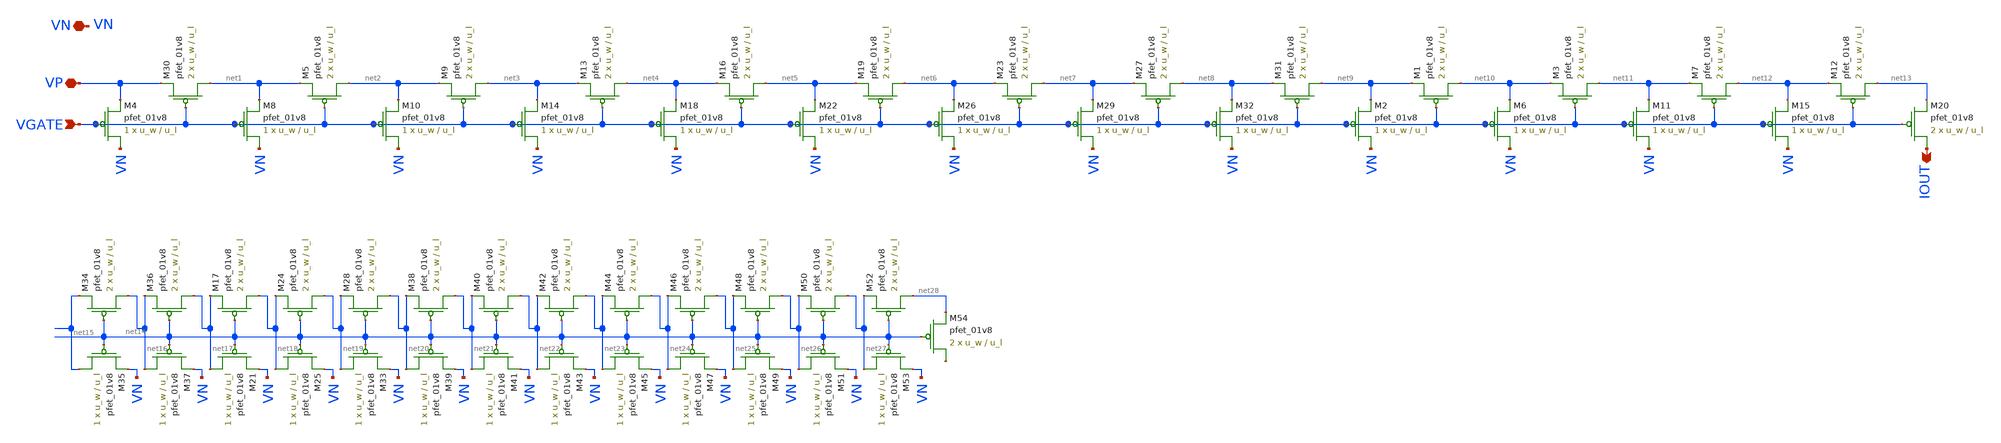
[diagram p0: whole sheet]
** sch_path: lib/analog/schematic/current_divider_original.sch
**.subckt current_divider_original VGATE VP VN IOUT
*.ipin VGATE
*.iopin VP
*.iopin VN
*.opin IOUT
XM30 net1 VGATE VP VDD sky130_fd_pr__pfet_01v8 L=u_l W=u_w nf=1 ad='int((nf+1)/2) * W/nf * 0.29' as='int((nf+2)/2) * W/nf * 0.29'
+ pd='2*int((nf+1)/2) * (W/nf + 0.29)' ps='2*int((nf+2)/2) * (W/nf + 0.29)' nrd='0.29 / W' nrs='0.29 / W'
+ sa=0 sb=0 sd=0 mult=2 m=2
XM4 VN VGATE VP VDD sky130_fd_pr__pfet_01v8 L=u_l W=u_w nf=1 ad='int((nf+1)/2) * W/nf * 0.29' as='int((nf+2)/2) * W/nf * 0.29'
+ pd='2*int((nf+1)/2) * (W/nf + 0.29)' ps='2*int((nf+2)/2) * (W/nf + 0.29)' nrd='0.29 / W' nrs='0.29 / W'
+ sa=0 sb=0 sd=0 mult=1 m=1
XM5 net2 VGATE net1 VDD sky130_fd_pr__pfet_01v8 L=u_l W=u_w nf=1 ad='int((nf+1)/2) * W/nf * 0.29' as='int((nf+2)/2) * W/nf * 0.29'
+ pd='2*int((nf+1)/2) * (W/nf + 0.29)' ps='2*int((nf+2)/2) * (W/nf + 0.29)' nrd='0.29 / W' nrs='0.29 / W'
+ sa=0 sb=0 sd=0 mult=2 m=2
XM8 VN VGATE net1 VDD sky130_fd_pr__pfet_01v8 L=u_l W=u_w nf=1 ad='int((nf+1)/2) * W/nf * 0.29' as='int((nf+2)/2) * W/nf * 0.29'
+ pd='2*int((nf+1)/2) * (W/nf + 0.29)' ps='2*int((nf+2)/2) * (W/nf + 0.29)' nrd='0.29 / W' nrs='0.29 / W'
+ sa=0 sb=0 sd=0 mult=1 m=1
XM9 net3 VGATE net2 VDD sky130_fd_pr__pfet_01v8 L=u_l W=u_w nf=1 ad='int((nf+1)/2) * W/nf * 0.29' as='int((nf+2)/2) * W/nf * 0.29'
+ pd='2*int((nf+1)/2) * (W/nf + 0.29)' ps='2*int((nf+2)/2) * (W/nf + 0.29)' nrd='0.29 / W' nrs='0.29 / W'
+ sa=0 sb=0 sd=0 mult=2 m=2
XM10 VN VGATE net2 VDD sky130_fd_pr__pfet_01v8 L=u_l W=u_w nf=1 ad='int((nf+1)/2) * W/nf * 0.29' as='int((nf+2)/2) * W/nf * 0.29'
+ pd='2*int((nf+1)/2) * (W/nf + 0.29)' ps='2*int((nf+2)/2) * (W/nf + 0.29)' nrd='0.29 / W' nrs='0.29 / W'
+ sa=0 sb=0 sd=0 mult=1 m=1
XM13 net4 VGATE net3 VDD sky130_fd_pr__pfet_01v8 L=u_l W=u_w nf=1 ad='int((nf+1)/2) * W/nf * 0.29' as='int((nf+2)/2) * W/nf * 0.29'
+ pd='2*int((nf+1)/2) * (W/nf + 0.29)' ps='2*int((nf+2)/2) * (W/nf + 0.29)' nrd='0.29 / W' nrs='0.29 / W'
+ sa=0 sb=0 sd=0 mult=2 m=2
XM14 VN VGATE net3 VDD sky130_fd_pr__pfet_01v8 L=u_l W=u_w nf=1 ad='int((nf+1)/2) * W/nf * 0.29' as='int((nf+2)/2) * W/nf * 0.29'
+ pd='2*int((nf+1)/2) * (W/nf + 0.29)' ps='2*int((nf+2)/2) * (W/nf + 0.29)' nrd='0.29 / W' nrs='0.29 / W'
+ sa=0 sb=0 sd=0 mult=1 m=1
XM16 net5 VGATE net4 VDD sky130_fd_pr__pfet_01v8 L=u_l W=u_w nf=1 ad='int((nf+1)/2) * W/nf * 0.29' as='int((nf+2)/2) * W/nf * 0.29'
+ pd='2*int((nf+1)/2) * (W/nf + 0.29)' ps='2*int((nf+2)/2) * (W/nf + 0.29)' nrd='0.29 / W' nrs='0.29 / W'
+ sa=0 sb=0 sd=0 mult=2 m=2
XM18 VN VGATE net4 VDD sky130_fd_pr__pfet_01v8 L=u_l W=u_w nf=1 ad='int((nf+1)/2) * W/nf * 0.29' as='int((nf+2)/2) * W/nf * 0.29'
+ pd='2*int((nf+1)/2) * (W/nf + 0.29)' ps='2*int((nf+2)/2) * (W/nf + 0.29)' nrd='0.29 / W' nrs='0.29 / W'
+ sa=0 sb=0 sd=0 mult=1 m=1
XM19 net6 VGATE net5 VDD sky130_fd_pr__pfet_01v8 L=u_l W=u_w nf=1 ad='int((nf+1)/2) * W/nf * 0.29' as='int((nf+2)/2) * W/nf * 0.29'
+ pd='2*int((nf+1)/2) * (W/nf + 0.29)' ps='2*int((nf+2)/2) * (W/nf + 0.29)' nrd='0.29 / W' nrs='0.29 / W'
+ sa=0 sb=0 sd=0 mult=2 m=2
XM22 VN VGATE net5 VDD sky130_fd_pr__pfet_01v8 L=u_l W=u_w nf=1 ad='int((nf+1)/2) * W/nf * 0.29' as='int((nf+2)/2) * W/nf * 0.29'
+ pd='2*int((nf+1)/2) * (W/nf + 0.29)' ps='2*int((nf+2)/2) * (W/nf + 0.29)' nrd='0.29 / W' nrs='0.29 / W'
+ sa=0 sb=0 sd=0 mult=1 m=1
XM23 net7 VGATE net6 VDD sky130_fd_pr__pfet_01v8 L=u_l W=u_w nf=1 ad='int((nf+1)/2) * W/nf * 0.29' as='int((nf+2)/2) * W/nf * 0.29'
+ pd='2*int((nf+1)/2) * (W/nf + 0.29)' ps='2*int((nf+2)/2) * (W/nf + 0.29)' nrd='0.29 / W' nrs='0.29 / W'
+ sa=0 sb=0 sd=0 mult=2 m=2
XM26 VN VGATE net6 VDD sky130_fd_pr__pfet_01v8 L=u_l W=u_w nf=1 ad='int((nf+1)/2) * W/nf * 0.29' as='int((nf+2)/2) * W/nf * 0.29'
+ pd='2*int((nf+1)/2) * (W/nf + 0.29)' ps='2*int((nf+2)/2) * (W/nf + 0.29)' nrd='0.29 / W' nrs='0.29 / W'
+ sa=0 sb=0 sd=0 mult=1 m=1
XM27 net8 VGATE net7 VDD sky130_fd_pr__pfet_01v8 L=u_l W=u_w nf=1 ad='int((nf+1)/2) * W/nf * 0.29' as='int((nf+2)/2) * W/nf * 0.29'
+ pd='2*int((nf+1)/2) * (W/nf + 0.29)' ps='2*int((nf+2)/2) * (W/nf + 0.29)' nrd='0.29 / W' nrs='0.29 / W'
+ sa=0 sb=0 sd=0 mult=2 m=2
XM29 VN VGATE net7 VDD sky130_fd_pr__pfet_01v8 L=u_l W=u_w nf=1 ad='int((nf+1)/2) * W/nf * 0.29' as='int((nf+2)/2) * W/nf * 0.29'
+ pd='2*int((nf+1)/2) * (W/nf + 0.29)' ps='2*int((nf+2)/2) * (W/nf + 0.29)' nrd='0.29 / W' nrs='0.29 / W'
+ sa=0 sb=0 sd=0 mult=1 m=1
XM31 net9 VGATE net8 VDD sky130_fd_pr__pfet_01v8 L=u_l W=u_w nf=1 ad='int((nf+1)/2) * W/nf * 0.29' as='int((nf+2)/2) * W/nf * 0.29'
+ pd='2*int((nf+1)/2) * (W/nf + 0.29)' ps='2*int((nf+2)/2) * (W/nf + 0.29)' nrd='0.29 / W' nrs='0.29 / W'
+ sa=0 sb=0 sd=0 mult=2 m=2
XM32 VN VGATE net8 VDD sky130_fd_pr__pfet_01v8 L=u_l W=u_w nf=1 ad='int((nf+1)/2) * W/nf * 0.29' as='int((nf+2)/2) * W/nf * 0.29'
+ pd='2*int((nf+1)/2) * (W/nf + 0.29)' ps='2*int((nf+2)/2) * (W/nf + 0.29)' nrd='0.29 / W' nrs='0.29 / W'
+ sa=0 sb=0 sd=0 mult=1 m=1
XM1 net10 VGATE net9 VDD sky130_fd_pr__pfet_01v8 L=u_l W=u_w nf=1 ad='int((nf+1)/2) * W/nf * 0.29' as='int((nf+2)/2) * W/nf * 0.29'
+ pd='2*int((nf+1)/2) * (W/nf + 0.29)' ps='2*int((nf+2)/2) * (W/nf + 0.29)' nrd='0.29 / W' nrs='0.29 / W'
+ sa=0 sb=0 sd=0 mult=2 m=2
XM2 VN VGATE net9 VDD sky130_fd_pr__pfet_01v8 L=u_l W=u_w nf=1 ad='int((nf+1)/2) * W/nf * 0.29' as='int((nf+2)/2) * W/nf * 0.29'
+ pd='2*int((nf+1)/2) * (W/nf + 0.29)' ps='2*int((nf+2)/2) * (W/nf + 0.29)' nrd='0.29 / W' nrs='0.29 / W'
+ sa=0 sb=0 sd=0 mult=1 m=1
XM3 net11 VGATE net10 VDD sky130_fd_pr__pfet_01v8 L=u_l W=u_w nf=1 ad='int((nf+1)/2) * W/nf * 0.29' as='int((nf+2)/2) * W/nf * 0.29'
+ pd='2*int((nf+1)/2) * (W/nf + 0.29)' ps='2*int((nf+2)/2) * (W/nf + 0.29)' nrd='0.29 / W' nrs='0.29 / W'
+ sa=0 sb=0 sd=0 mult=2 m=2
XM6 VN VGATE net10 VDD sky130_fd_pr__pfet_01v8 L=u_l W=u_w nf=1 ad='int((nf+1)/2) * W/nf * 0.29' as='int((nf+2)/2) * W/nf * 0.29'
+ pd='2*int((nf+1)/2) * (W/nf + 0.29)' ps='2*int((nf+2)/2) * (W/nf + 0.29)' nrd='0.29 / W' nrs='0.29 / W'
+ sa=0 sb=0 sd=0 mult=1 m=1
XM7 net12 VGATE net11 VDD sky130_fd_pr__pfet_01v8 L=u_l W=u_w nf=1 ad='int((nf+1)/2) * W/nf * 0.29' as='int((nf+2)/2) * W/nf * 0.29'
+ pd='2*int((nf+1)/2) * (W/nf + 0.29)' ps='2*int((nf+2)/2) * (W/nf + 0.29)' nrd='0.29 / W' nrs='0.29 / W'
+ sa=0 sb=0 sd=0 mult=2 m=2
XM11 VN VGATE net11 VDD sky130_fd_pr__pfet_01v8 L=u_l W=u_w nf=1 ad='int((nf+1)/2) * W/nf * 0.29' as='int((nf+2)/2) * W/nf * 0.29'
+ pd='2*int((nf+1)/2) * (W/nf + 0.29)' ps='2*int((nf+2)/2) * (W/nf + 0.29)' nrd='0.29 / W' nrs='0.29 / W'
+ sa=0 sb=0 sd=0 mult=1 m=1
XM12 net13 VGATE net12 VDD sky130_fd_pr__pfet_01v8 L=u_l W=u_w nf=1 ad='int((nf+1)/2) * W/nf * 0.29'
+ as='int((nf+2)/2) * W/nf * 0.29' pd='2*int((nf+1)/2) * (W/nf + 0.29)' ps='2*int((nf+2)/2) * (W/nf + 0.29)'
+ nrd='0.29 / W' nrs='0.29 / W' sa=0 sb=0 sd=0 mult=2 m=2
XM15 VN VGATE net12 VDD sky130_fd_pr__pfet_01v8 L=u_l W=u_w nf=1 ad='int((nf+1)/2) * W/nf * 0.29' as='int((nf+2)/2) * W/nf * 0.29'
+ pd='2*int((nf+1)/2) * (W/nf + 0.29)' ps='2*int((nf+2)/2) * (W/nf + 0.29)' nrd='0.29 / W' nrs='0.29 / W'
+ sa=0 sb=0 sd=0 mult=1 m=1
XM20 IOUT VGATE net13 VDD sky130_fd_pr__pfet_01v8 L=u_l W=u_w nf=1 ad='int((nf+1)/2) * W/nf * 0.29' as='int((nf+2)/2) * W/nf * 0.29'
+ pd='2*int((nf+1)/2) * (W/nf + 0.29)' ps='2*int((nf+2)/2) * (W/nf + 0.29)' nrd='0.29 / W' nrs='0.29 / W'
+ sa=0 sb=0 sd=0 mult=2 m=2
XM34 net16 net14 net15 VDD sky130_fd_pr__pfet_01v8 L=u_l W=u_w nf=1 ad='int((nf+1)/2) * W/nf * 0.29'
+ as='int((nf+2)/2) * W/nf * 0.29' pd='2*int((nf+1)/2) * (W/nf + 0.29)' ps='2*int((nf+2)/2) * (W/nf + 0.29)'
+ nrd='0.29 / W' nrs='0.29 / W' sa=0 sb=0 sd=0 mult=2 m=2
XM35 net15 net14 VN VDD sky130_fd_pr__pfet_01v8 L=u_l W=u_w nf=1 ad='int((nf+1)/2) * W/nf * 0.29' as='int((nf+2)/2) * W/nf * 0.29'
+ pd='2*int((nf+1)/2) * (W/nf + 0.29)' ps='2*int((nf+2)/2) * (W/nf + 0.29)' nrd='0.29 / W' nrs='0.29 / W'
+ sa=0 sb=0 sd=0 mult=1 m=1
XM36 net17 net14 net16 VDD sky130_fd_pr__pfet_01v8 L=u_l W=u_w nf=1 ad='int((nf+1)/2) * W/nf * 0.29'
+ as='int((nf+2)/2) * W/nf * 0.29' pd='2*int((nf+1)/2) * (W/nf + 0.29)' ps='2*int((nf+2)/2) * (W/nf + 0.29)'
+ nrd='0.29 / W' nrs='0.29 / W' sa=0 sb=0 sd=0 mult=2 m=2
XM37 net16 net14 VN VDD sky130_fd_pr__pfet_01v8 L=u_l W=u_w nf=1 ad='int((nf+1)/2) * W/nf * 0.29' as='int((nf+2)/2) * W/nf * 0.29'
+ pd='2*int((nf+1)/2) * (W/nf + 0.29)' ps='2*int((nf+2)/2) * (W/nf + 0.29)' nrd='0.29 / W' nrs='0.29 / W'
+ sa=0 sb=0 sd=0 mult=1 m=1
XM17 net18 net14 net17 VDD sky130_fd_pr__pfet_01v8 L=u_l W=u_w nf=1 ad='int((nf+1)/2) * W/nf * 0.29'
+ as='int((nf+2)/2) * W/nf * 0.29' pd='2*int((nf+1)/2) * (W/nf + 0.29)' ps='2*int((nf+2)/2) * (W/nf + 0.29)'
+ nrd='0.29 / W' nrs='0.29 / W' sa=0 sb=0 sd=0 mult=2 m=2
XM21 net17 net14 VN VDD sky130_fd_pr__pfet_01v8 L=u_l W=u_w nf=1 ad='int((nf+1)/2) * W/nf * 0.29' as='int((nf+2)/2) * W/nf * 0.29'
+ pd='2*int((nf+1)/2) * (W/nf + 0.29)' ps='2*int((nf+2)/2) * (W/nf + 0.29)' nrd='0.29 / W' nrs='0.29 / W'
+ sa=0 sb=0 sd=0 mult=1 m=1
XM24 net19 net14 net18 VDD sky130_fd_pr__pfet_01v8 L=u_l W=u_w nf=1 ad='int((nf+1)/2) * W/nf * 0.29'
+ as='int((nf+2)/2) * W/nf * 0.29' pd='2*int((nf+1)/2) * (W/nf + 0.29)' ps='2*int((nf+2)/2) * (W/nf + 0.29)'
+ nrd='0.29 / W' nrs='0.29 / W' sa=0 sb=0 sd=0 mult=2 m=2
XM25 net18 net14 VN VDD sky130_fd_pr__pfet_01v8 L=u_l W=u_w nf=1 ad='int((nf+1)/2) * W/nf * 0.29' as='int((nf+2)/2) * W/nf * 0.29'
+ pd='2*int((nf+1)/2) * (W/nf + 0.29)' ps='2*int((nf+2)/2) * (W/nf + 0.29)' nrd='0.29 / W' nrs='0.29 / W'
+ sa=0 sb=0 sd=0 mult=1 m=1
XM28 net20 net14 net19 VDD sky130_fd_pr__pfet_01v8 L=u_l W=u_w nf=1 ad='int((nf+1)/2) * W/nf * 0.29'
+ as='int((nf+2)/2) * W/nf * 0.29' pd='2*int((nf+1)/2) * (W/nf + 0.29)' ps='2*int((nf+2)/2) * (W/nf + 0.29)'
+ nrd='0.29 / W' nrs='0.29 / W' sa=0 sb=0 sd=0 mult=2 m=2
XM33 net19 net14 VN VDD sky130_fd_pr__pfet_01v8 L=u_l W=u_w nf=1 ad='int((nf+1)/2) * W/nf * 0.29' as='int((nf+2)/2) * W/nf * 0.29'
+ pd='2*int((nf+1)/2) * (W/nf + 0.29)' ps='2*int((nf+2)/2) * (W/nf + 0.29)' nrd='0.29 / W' nrs='0.29 / W'
+ sa=0 sb=0 sd=0 mult=1 m=1
XM38 net21 net14 net20 VDD sky130_fd_pr__pfet_01v8 L=u_l W=u_w nf=1 ad='int((nf+1)/2) * W/nf * 0.29'
+ as='int((nf+2)/2) * W/nf * 0.29' pd='2*int((nf+1)/2) * (W/nf + 0.29)' ps='2*int((nf+2)/2) * (W/nf + 0.29)'
+ nrd='0.29 / W' nrs='0.29 / W' sa=0 sb=0 sd=0 mult=2 m=2
XM39 net20 net14 VN VDD sky130_fd_pr__pfet_01v8 L=u_l W=u_w nf=1 ad='int((nf+1)/2) * W/nf * 0.29' as='int((nf+2)/2) * W/nf * 0.29'
+ pd='2*int((nf+1)/2) * (W/nf + 0.29)' ps='2*int((nf+2)/2) * (W/nf + 0.29)' nrd='0.29 / W' nrs='0.29 / W'
+ sa=0 sb=0 sd=0 mult=1 m=1
XM40 net22 net14 net21 VDD sky130_fd_pr__pfet_01v8 L=u_l W=u_w nf=1 ad='int((nf+1)/2) * W/nf * 0.29'
+ as='int((nf+2)/2) * W/nf * 0.29' pd='2*int((nf+1)/2) * (W/nf + 0.29)' ps='2*int((nf+2)/2) * (W/nf + 0.29)'
+ nrd='0.29 / W' nrs='0.29 / W' sa=0 sb=0 sd=0 mult=2 m=2
XM41 net21 net14 VN VDD sky130_fd_pr__pfet_01v8 L=u_l W=u_w nf=1 ad='int((nf+1)/2) * W/nf * 0.29' as='int((nf+2)/2) * W/nf * 0.29'
+ pd='2*int((nf+1)/2) * (W/nf + 0.29)' ps='2*int((nf+2)/2) * (W/nf + 0.29)' nrd='0.29 / W' nrs='0.29 / W'
+ sa=0 sb=0 sd=0 mult=1 m=1
XM42 net23 net14 net22 VDD sky130_fd_pr__pfet_01v8 L=u_l W=u_w nf=1 ad='int((nf+1)/2) * W/nf * 0.29'
+ as='int((nf+2)/2) * W/nf * 0.29' pd='2*int((nf+1)/2) * (W/nf + 0.29)' ps='2*int((nf+2)/2) * (W/nf + 0.29)'
+ nrd='0.29 / W' nrs='0.29 / W' sa=0 sb=0 sd=0 mult=2 m=2
XM43 net22 net14 VN VDD sky130_fd_pr__pfet_01v8 L=u_l W=u_w nf=1 ad='int((nf+1)/2) * W/nf * 0.29' as='int((nf+2)/2) * W/nf * 0.29'
+ pd='2*int((nf+1)/2) * (W/nf + 0.29)' ps='2*int((nf+2)/2) * (W/nf + 0.29)' nrd='0.29 / W' nrs='0.29 / W'
+ sa=0 sb=0 sd=0 mult=1 m=1
XM44 net24 net14 net23 VDD sky130_fd_pr__pfet_01v8 L=u_l W=u_w nf=1 ad='int((nf+1)/2) * W/nf * 0.29'
+ as='int((nf+2)/2) * W/nf * 0.29' pd='2*int((nf+1)/2) * (W/nf + 0.29)' ps='2*int((nf+2)/2) * (W/nf + 0.29)'
+ nrd='0.29 / W' nrs='0.29 / W' sa=0 sb=0 sd=0 mult=2 m=2
XM45 net23 net14 VN VDD sky130_fd_pr__pfet_01v8 L=u_l W=u_w nf=1 ad='int((nf+1)/2) * W/nf * 0.29' as='int((nf+2)/2) * W/nf * 0.29'
+ pd='2*int((nf+1)/2) * (W/nf + 0.29)' ps='2*int((nf+2)/2) * (W/nf + 0.29)' nrd='0.29 / W' nrs='0.29 / W'
+ sa=0 sb=0 sd=0 mult=1 m=1
XM46 net25 net14 net24 VDD sky130_fd_pr__pfet_01v8 L=u_l W=u_w nf=1 ad='int((nf+1)/2) * W/nf * 0.29'
+ as='int((nf+2)/2) * W/nf * 0.29' pd='2*int((nf+1)/2) * (W/nf + 0.29)' ps='2*int((nf+2)/2) * (W/nf + 0.29)'
+ nrd='0.29 / W' nrs='0.29 / W' sa=0 sb=0 sd=0 mult=2 m=2
XM47 net24 net14 VN VDD sky130_fd_pr__pfet_01v8 L=u_l W=u_w nf=1 ad='int((nf+1)/2) * W/nf * 0.29' as='int((nf+2)/2) * W/nf * 0.29'
+ pd='2*int((nf+1)/2) * (W/nf + 0.29)' ps='2*int((nf+2)/2) * (W/nf + 0.29)' nrd='0.29 / W' nrs='0.29 / W'
+ sa=0 sb=0 sd=0 mult=1 m=1
XM48 net26 net14 net25 VDD sky130_fd_pr__pfet_01v8 L=u_l W=u_w nf=1 ad='int((nf+1)/2) * W/nf * 0.29'
+ as='int((nf+2)/2) * W/nf * 0.29' pd='2*int((nf+1)/2) * (W/nf + 0.29)' ps='2*int((nf+2)/2) * (W/nf + 0.29)'
+ nrd='0.29 / W' nrs='0.29 / W' sa=0 sb=0 sd=0 mult=2 m=2
XM49 net25 net14 VN VDD sky130_fd_pr__pfet_01v8 L=u_l W=u_w nf=1 ad='int((nf+1)/2) * W/nf * 0.29' as='int((nf+2)/2) * W/nf * 0.29'
+ pd='2*int((nf+1)/2) * (W/nf + 0.29)' ps='2*int((nf+2)/2) * (W/nf + 0.29)' nrd='0.29 / W' nrs='0.29 / W'
+ sa=0 sb=0 sd=0 mult=1 m=1
XM50 net27 net14 net26 VDD sky130_fd_pr__pfet_01v8 L=u_l W=u_w nf=1 ad='int((nf+1)/2) * W/nf * 0.29'
+ as='int((nf+2)/2) * W/nf * 0.29' pd='2*int((nf+1)/2) * (W/nf + 0.29)' ps='2*int((nf+2)/2) * (W/nf + 0.29)'
+ nrd='0.29 / W' nrs='0.29 / W' sa=0 sb=0 sd=0 mult=2 m=2
XM51 net26 net14 VN VDD sky130_fd_pr__pfet_01v8 L=u_l W=u_w nf=1 ad='int((nf+1)/2) * W/nf * 0.29' as='int((nf+2)/2) * W/nf * 0.29'
+ pd='2*int((nf+1)/2) * (W/nf + 0.29)' ps='2*int((nf+2)/2) * (W/nf + 0.29)' nrd='0.29 / W' nrs='0.29 / W'
+ sa=0 sb=0 sd=0 mult=1 m=1
XM52 net28 net14 net27 VDD sky130_fd_pr__pfet_01v8 L=u_l W=u_w nf=1 ad='int((nf+1)/2) * W/nf * 0.29'
+ as='int((nf+2)/2) * W/nf * 0.29' pd='2*int((nf+1)/2) * (W/nf + 0.29)' ps='2*int((nf+2)/2) * (W/nf + 0.29)'
+ nrd='0.29 / W' nrs='0.29 / W' sa=0 sb=0 sd=0 mult=2 m=2
XM53 net27 net14 VN VDD sky130_fd_pr__pfet_01v8 L=u_l W=u_w nf=1 ad='int((nf+1)/2) * W/nf * 0.29' as='int((nf+2)/2) * W/nf * 0.29'
+ pd='2*int((nf+1)/2) * (W/nf + 0.29)' ps='2*int((nf+2)/2) * (W/nf + 0.29)' nrd='0.29 / W' nrs='0.29 / W'
+ sa=0 sb=0 sd=0 mult=1 m=1
XM54 net29 net14 net28 VDD sky130_fd_pr__pfet_01v8 L=u_l W=u_w nf=1 ad='int((nf+1)/2) * W/nf * 0.29'
+ as='int((nf+2)/2) * W/nf * 0.29' pd='2*int((nf+1)/2) * (W/nf + 0.29)' ps='2*int((nf+2)/2) * (W/nf + 0.29)'
+ nrd='0.29 / W' nrs='0.29 / W' sa=0 sb=0 sd=0 mult=2 m=2
**.ends
.end
